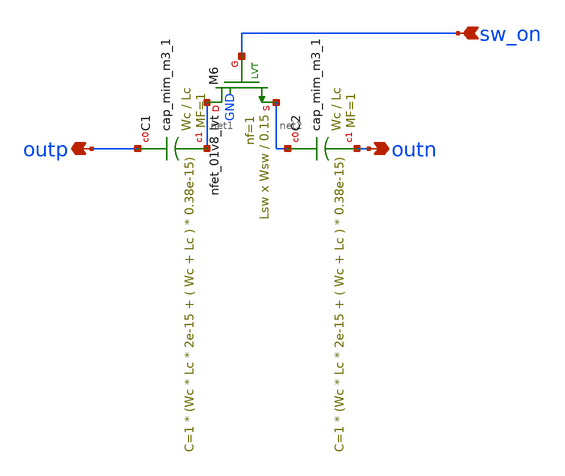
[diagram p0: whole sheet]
** sch_path: openfasoc/generators/lc-dco/xschem_rundir/swcap_2C1M.sch
**.subckt swcap_2C1M outn outp sw_on
*.opin outn
*.opin outp
*.ipin sw_on
XC1 outp net1 sky130_fd_pr__cap_mim_m3_1 W=Wc L=Lc MF=1 m=1
XC2 net2 outn sky130_fd_pr__cap_mim_m3_1 W=Wc L=Lc MF=1 m=1
XM6 net1 sw_on net2 GND sky130_fd_pr__nfet_01v8_lvt L=0.15 W=Wsw nf=1 ad='int((nf+1)/2) * W/nf * 0.29'
+ as='int((nf+2)/2) * W/nf * 0.29' pd='2*int((nf+1)/2) * (W/nf + 0.29)' ps='2*int((nf+2)/2) * (W/nf + 0.29)'
+ nrd='0.29 / W' nrs='0.29 / W' sa=0 sb=0 sd=0 mult=Lsw m=Lsw
**.ends
.end
